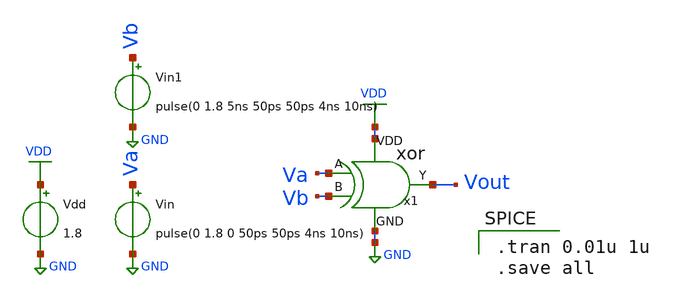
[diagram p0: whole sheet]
** sch_path: designs/xor12t/xschem/xor_tb.sch
**.subckt xor_tb
Vdd VDD GND 1.8
Vin Va GND pulse(0 1.8 0 50ps 50ps 4ns 10ns)
Vin1 Vb GND pulse(0 1.8 5ns 50ps 50ps 4ns 10ns)
x1 VDD Va Vout Vb GND xor
**** begin user architecture code

** opencircuidesign pdks install
.lib /home/ubvm/Desktop/chip_design/open_pdks/sky130/sky130A/libs.tech/ngspice/sky130.lib.spice tt_mm




.tran 0.01u 1u
.save all

**** end user architecture code
**.ends

* expanding   symbol:  /home/ubvm/unic-cass/xor/xor.sym # of pins=5
** sym_path: designs/xor12t/xschem/xor.sym
** sch_path: designs/xor12t/xschem/xor.sch
.subckt xor VDD A Y B GND
*.ipin A
*.ipin B
*.opin Y
*.iopin GND
*.iopin VDD
XM1 net1 A GND GND sky130_fd_pr__nfet_01v8 L=0.15 W=1 nf=1 ad='int((1 + 1)/2) * 1 / 1 * 0.29' as='int((1 + 2)/2) * 1 / 1 * 0.29'
+ pd='2*int((1 + 1)/2) * (1 / 1 + 0.29)' ps='2*int((1 + 2)/2) * (1 / 1 + 0.29)' nrd='0.29 / 1 ' nrs='0.29 / 1 '
+ sa=0 sb=0 sd=0 mult=1 m=1
XM2 net1 A VDD VDD sky130_fd_pr__pfet_01v8 L=0.15 W=1 nf=1 ad='int((1 + 1)/2) * 1 / 1 * 0.29' as='int((1 + 2)/2) * 1 / 1 * 0.29'
+ pd='2*int((1 + 1)/2) * (1 / 1 + 0.29)' ps='2*int((1 + 2)/2) * (1 / 1 + 0.29)' nrd='0.29 / 1 ' nrs='0.29 / 1 '
+ sa=0 sb=0 sd=0 mult=1 m=1
XM3 net6 B GND GND sky130_fd_pr__nfet_01v8 L=0.15 W=1 nf=1 ad='int((1 + 1)/2) * 1 / 1 * 0.29' as='int((1 + 2)/2) * 1 / 1 * 0.29'
+ pd='2*int((1 + 1)/2) * (1 / 1 + 0.29)' ps='2*int((1 + 2)/2) * (1 / 1 + 0.29)' nrd='0.29 / 1 ' nrs='0.29 / 1 '
+ sa=0 sb=0 sd=0 mult=1 m=1
XM4 net6 B VDD VDD sky130_fd_pr__pfet_01v8 L=0.15 W=1 nf=1 ad='int((1 + 1)/2) * 1 / 1 * 0.29' as='int((1 + 2)/2) * 1 / 1 * 0.29'
+ pd='2*int((1 + 1)/2) * (1 / 1 + 0.29)' ps='2*int((1 + 2)/2) * (1 / 1 + 0.29)' nrd='0.29 / 1 ' nrs='0.29 / 1 '
+ sa=0 sb=0 sd=0 mult=1 m=1
XM5 net5 net1 VDD VDD sky130_fd_pr__pfet_01v8 L=0.15 W=1 nf=1 ad='int((1 + 1)/2) * 1 / 1 * 0.29' as='int((1 + 2)/2) * 1 / 1 * 0.29'
+ pd='2*int((1 + 1)/2) * (1 / 1 + 0.29)' ps='2*int((1 + 2)/2) * (1 / 1 + 0.29)' nrd='0.29 / 1 ' nrs='0.29 / 1 '
+ sa=0 sb=0 sd=0 mult=1 m=1
XM6 Y B net5 net5 sky130_fd_pr__pfet_01v8 L=0.15 W=1 nf=1 ad='int((1 + 1)/2) * 1 / 1 * 0.29' as='int((1 + 2)/2) * 1 / 1 * 0.29'
+ pd='2*int((1 + 1)/2) * (1 / 1 + 0.29)' ps='2*int((1 + 2)/2) * (1 / 1 + 0.29)' nrd='0.29 / 1 ' nrs='0.29 / 1 '
+ sa=0 sb=0 sd=0 mult=1 m=1
XM7 Y A net2 net2 sky130_fd_pr__nfet_01v8 L=0.15 W=1 nf=1 ad='int((1 + 1)/2) * 1 / 1 * 0.29' as='int((1 + 2)/2) * 1 / 1 * 0.29'
+ pd='2*int((1 + 1)/2) * (1 / 1 + 0.29)' ps='2*int((1 + 2)/2) * (1 / 1 + 0.29)' nrd='0.29 / 1 ' nrs='0.29 / 1 '
+ sa=0 sb=0 sd=0 mult=1 m=1
XM8 net2 B GND GND sky130_fd_pr__nfet_01v8 L=0.15 W=1 nf=1 ad='int((1 + 1)/2) * 1 / 1 * 0.29' as='int((1 + 2)/2) * 1 / 1 * 0.29'
+ pd='2*int((1 + 1)/2) * (1 / 1 + 0.29)' ps='2*int((1 + 2)/2) * (1 / 1 + 0.29)' nrd='0.29 / 1 ' nrs='0.29 / 1 '
+ sa=0 sb=0 sd=0 mult=1 m=1
XM9 net4 A VDD VDD sky130_fd_pr__pfet_01v8 L=0.15 W=1 nf=1 ad='int((1 + 1)/2) * 1 / 1 * 0.29' as='int((1 + 2)/2) * 1 / 1 * 0.29'
+ pd='2*int((1 + 1)/2) * (1 / 1 + 0.29)' ps='2*int((1 + 2)/2) * (1 / 1 + 0.29)' nrd='0.29 / 1 ' nrs='0.29 / 1 '
+ sa=0 sb=0 sd=0 mult=1 m=1
XM10 Y net6 net4 net4 sky130_fd_pr__pfet_01v8 L=0.15 W=1 nf=1 ad='int((1 + 1)/2) * 1 / 1 * 0.29' as='int((1 + 2)/2) * 1 / 1 * 0.29'
+ pd='2*int((1 + 1)/2) * (1 / 1 + 0.29)' ps='2*int((1 + 2)/2) * (1 / 1 + 0.29)' nrd='0.29 / 1 ' nrs='0.29 / 1 '
+ sa=0 sb=0 sd=0 mult=1 m=1
XM11 Y net1 net3 net3 sky130_fd_pr__nfet_01v8 L=0.15 W=1 nf=1 ad='int((1 + 1)/2) * 1 / 1 * 0.29' as='int((1 + 2)/2) * 1 / 1 * 0.29'
+ pd='2*int((1 + 1)/2) * (1 / 1 + 0.29)' ps='2*int((1 + 2)/2) * (1 / 1 + 0.29)' nrd='0.29 / 1 ' nrs='0.29 / 1 '
+ sa=0 sb=0 sd=0 mult=1 m=1
XM12 net3 net6 GND GND sky130_fd_pr__nfet_01v8 L=0.15 W=1 nf=1 ad='int((1 + 1)/2) * 1 / 1 * 0.29' as='int((1 + 2)/2) * 1 / 1 * 0.29'
+ pd='2*int((1 + 1)/2) * (1 / 1 + 0.29)' ps='2*int((1 + 2)/2) * (1 / 1 + 0.29)' nrd='0.29 / 1 ' nrs='0.29 / 1 '
+ sa=0 sb=0 sd=0 mult=1 m=1
.ends

.GLOBAL VDD
.GLOBAL GND
.end
